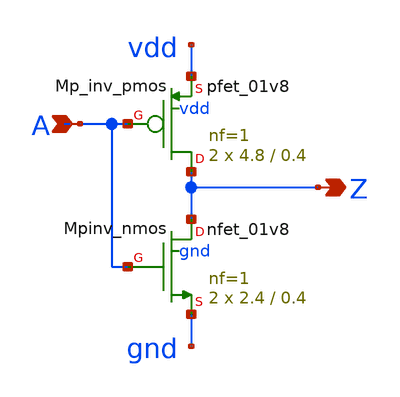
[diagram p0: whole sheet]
** sch_path: sram_4_16_scn4m/pinv_7.sch
**.subckt pinv_7 A Z
*.ipin A
*.opin Z
XMpinv_nmos Z A gnd gnd sky130_fd_pr__nfet_01v8 L=0.4 W=2.4 nf=1 ad='int((nf+1)/2) * W/nf * 0.29' as='int((nf+2)/2) * W/nf * 0.29'
+ pd='2*int((nf+1)/2) * (W/nf + 0.29)' ps='2*int((nf+2)/2) * (W/nf + 0.29)' nrd='0.29 / W' nrs='0.29 / W'
+ sa=0 sb=0 sd=0 mult=2 m=2
XMp_inv_pmos Z A vdd vdd sky130_fd_pr__pfet_01v8 L=0.4 W=4.8 nf=1 ad='int((nf+1)/2) * W/nf * 0.29' as='int((nf+2)/2) * W/nf * 0.29'
+ pd='2*int((nf+1)/2) * (W/nf + 0.29)' ps='2*int((nf+2)/2) * (W/nf + 0.29)' nrd='0.29 / W' nrs='0.29 / W'
+ sa=0 sb=0 sd=0 mult=2 m=2
**.ends
.end
